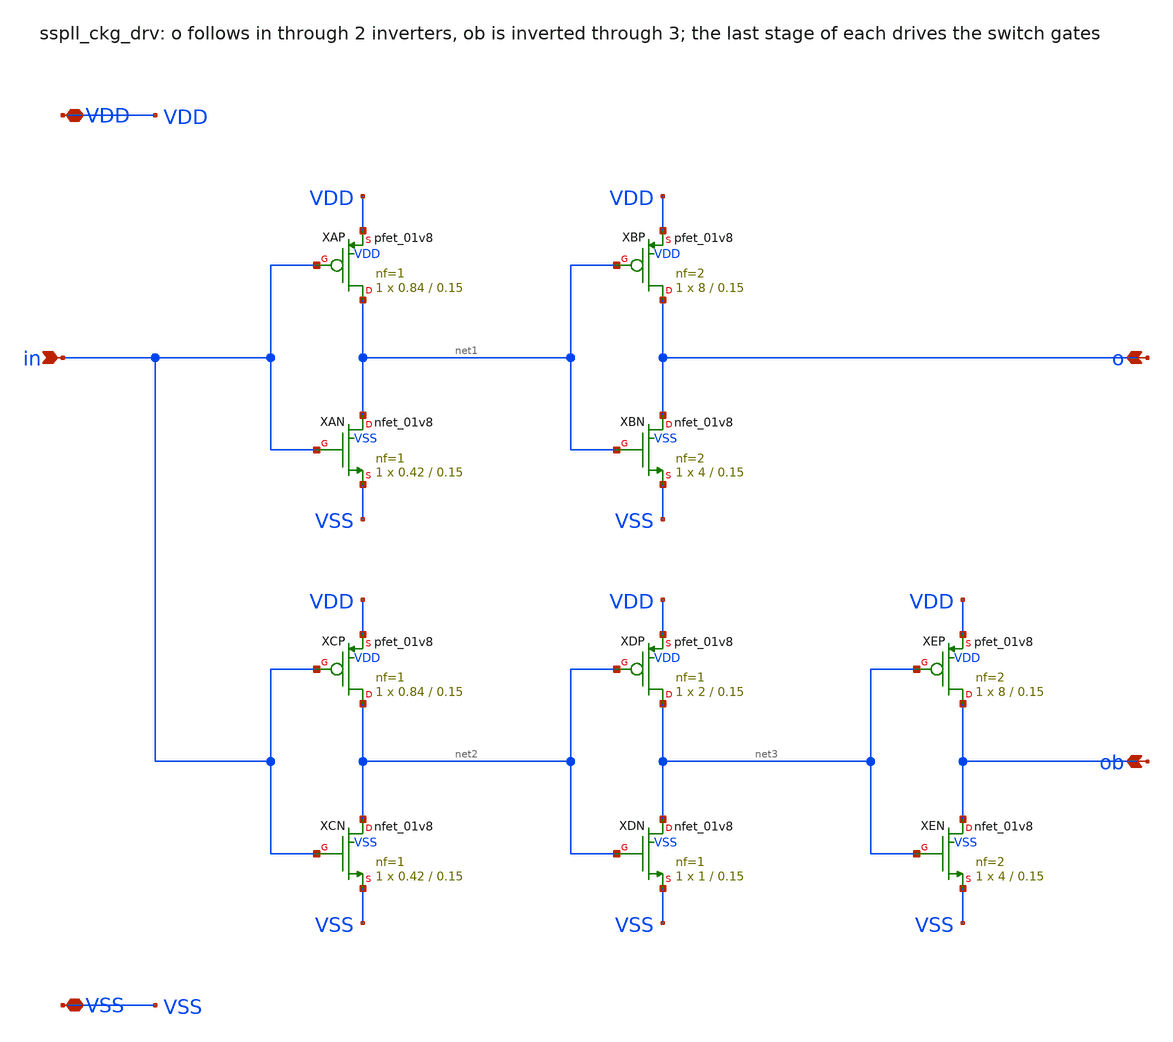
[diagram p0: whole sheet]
** sch_path: xschem/clkgen/sspll_ckg_drv.sch
**.subckt sspll_ckg_drv in o ob VDD VSS
*.ipin in
*.opin o
*.opin ob
*.iopin VDD
*.iopin VSS
XXAP net1 in VDD VDD sky130_fd_pr__pfet_01v8 L=0.15 W=0.84 nf=1 ad='int((nf+1)/2) * W/nf * 0.29' as='int((nf+2)/2) * W/nf * 0.29'
+ pd='2*int((nf+1)/2) * (W/nf + 0.29)' ps='2*int((nf+2)/2) * (W/nf + 0.29)' nrd='0.29 / W' nrs='0.29 / W'
+ sa=0 sb=0 sd=0 mult=1 m=1
XXAN net1 in VSS VSS sky130_fd_pr__nfet_01v8 L=0.15 W=0.42 nf=1 ad='int((nf+1)/2) * W/nf * 0.29' as='int((nf+2)/2) * W/nf * 0.29'
+ pd='2*int((nf+1)/2) * (W/nf + 0.29)' ps='2*int((nf+2)/2) * (W/nf + 0.29)' nrd='0.29 / W' nrs='0.29 / W'
+ sa=0 sb=0 sd=0 mult=1 m=1
XXBP o net1 VDD VDD sky130_fd_pr__pfet_01v8 L=0.15 W=8 nf=2 ad='int((nf+1)/2) * W/nf * 0.29' as='int((nf+2)/2) * W/nf * 0.29'
+ pd='2*int((nf+1)/2) * (W/nf + 0.29)' ps='2*int((nf+2)/2) * (W/nf + 0.29)' nrd='0.29 / W' nrs='0.29 / W'
+ sa=0 sb=0 sd=0 mult=1 m=1
XXBN o net1 VSS VSS sky130_fd_pr__nfet_01v8 L=0.15 W=4 nf=2 ad='int((nf+1)/2) * W/nf * 0.29' as='int((nf+2)/2) * W/nf * 0.29'
+ pd='2*int((nf+1)/2) * (W/nf + 0.29)' ps='2*int((nf+2)/2) * (W/nf + 0.29)' nrd='0.29 / W' nrs='0.29 / W'
+ sa=0 sb=0 sd=0 mult=1 m=1
XXCP net2 in VDD VDD sky130_fd_pr__pfet_01v8 L=0.15 W=0.84 nf=1 ad='int((nf+1)/2) * W/nf * 0.29' as='int((nf+2)/2) * W/nf * 0.29'
+ pd='2*int((nf+1)/2) * (W/nf + 0.29)' ps='2*int((nf+2)/2) * (W/nf + 0.29)' nrd='0.29 / W' nrs='0.29 / W'
+ sa=0 sb=0 sd=0 mult=1 m=1
XXCN net2 in VSS VSS sky130_fd_pr__nfet_01v8 L=0.15 W=0.42 nf=1 ad='int((nf+1)/2) * W/nf * 0.29' as='int((nf+2)/2) * W/nf * 0.29'
+ pd='2*int((nf+1)/2) * (W/nf + 0.29)' ps='2*int((nf+2)/2) * (W/nf + 0.29)' nrd='0.29 / W' nrs='0.29 / W'
+ sa=0 sb=0 sd=0 mult=1 m=1
XXDP net3 net2 VDD VDD sky130_fd_pr__pfet_01v8 L=0.15 W=2 nf=1 ad='int((nf+1)/2) * W/nf * 0.29' as='int((nf+2)/2) * W/nf * 0.29'
+ pd='2*int((nf+1)/2) * (W/nf + 0.29)' ps='2*int((nf+2)/2) * (W/nf + 0.29)' nrd='0.29 / W' nrs='0.29 / W'
+ sa=0 sb=0 sd=0 mult=1 m=1
XXDN net3 net2 VSS VSS sky130_fd_pr__nfet_01v8 L=0.15 W=1 nf=1 ad='int((nf+1)/2) * W/nf * 0.29' as='int((nf+2)/2) * W/nf * 0.29'
+ pd='2*int((nf+1)/2) * (W/nf + 0.29)' ps='2*int((nf+2)/2) * (W/nf + 0.29)' nrd='0.29 / W' nrs='0.29 / W'
+ sa=0 sb=0 sd=0 mult=1 m=1
XXEP ob net3 VDD VDD sky130_fd_pr__pfet_01v8 L=0.15 W=8 nf=2 ad='int((nf+1)/2) * W/nf * 0.29' as='int((nf+2)/2) * W/nf * 0.29'
+ pd='2*int((nf+1)/2) * (W/nf + 0.29)' ps='2*int((nf+2)/2) * (W/nf + 0.29)' nrd='0.29 / W' nrs='0.29 / W'
+ sa=0 sb=0 sd=0 mult=1 m=1
XXEN ob net3 VSS VSS sky130_fd_pr__nfet_01v8 L=0.15 W=4 nf=2 ad='int((nf+1)/2) * W/nf * 0.29' as='int((nf+2)/2) * W/nf * 0.29'
+ pd='2*int((nf+1)/2) * (W/nf + 0.29)' ps='2*int((nf+2)/2) * (W/nf + 0.29)' nrd='0.29 / W' nrs='0.29 / W'
+ sa=0 sb=0 sd=0 mult=1 m=1
**.ends
.end
